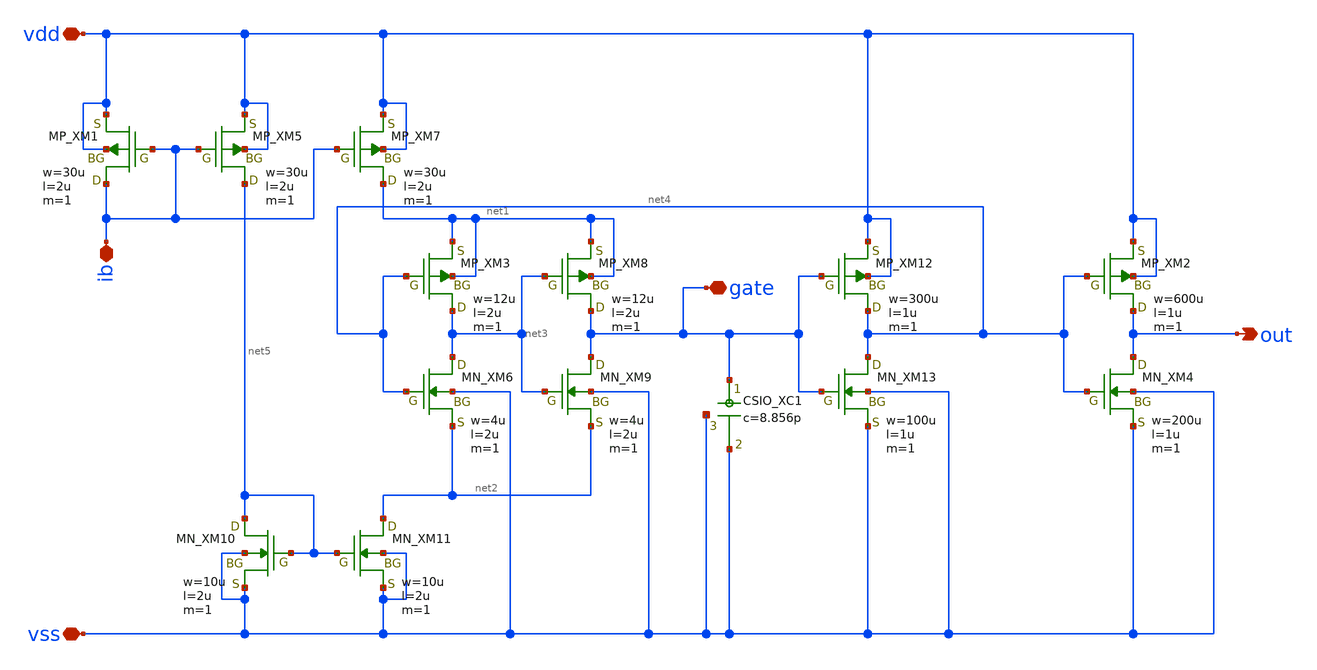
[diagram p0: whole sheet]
** sch_path: Vol.2/files/06/xschem/vco.sch
**.subckt vco out vdd vss ib gate
*.opin out
*.iopin vdd
*.iopin vss
*.iopin ib
*.iopin gate
XM1 ib ib vdd vdd PMOS w=30u l=2u as=0 ad=0 ps=0 pd=0 nrd=0 nrs=0 m=1
XM3 net3 net4 net1 net1 PMOS w=12u l=2u as=0 ad=0 ps=0 pd=0 nrd=0 nrs=0 m=1
XM6 net3 net4 net2 vss NMOS w=4u l=2u as=0 ad=0 ps=0 pd=0 nrd=0 nrs=0 m=1
XM7 net1 ib vdd vdd PMOS w=30u l=2u as=0 ad=0 ps=0 pd=0 nrd=0 nrs=0 m=1
XM8 gate net3 net1 net1 PMOS w=12u l=2u as=0 ad=0 ps=0 pd=0 nrd=0 nrs=0 m=1
XM9 gate net3 net2 vss NMOS w=4u l=2u as=0 ad=0 ps=0 pd=0 nrd=0 nrs=0 m=1
XM12 net4 gate vdd vdd PMOS w=300u l=1u as=0 ad=0 ps=0 pd=0 nrd=0 nrs=0 m=1
XM13 net4 gate vss vss NMOS w=100u l=1u as=0 ad=0 ps=0 pd=0 nrd=0 nrs=0 m=1
XM2 out net4 vdd vdd PMOS w=600u l=1u as=0 ad=0 ps=0 pd=0 nrd=0 nrs=0 m=1
XM4 out net4 vss vss NMOS w=200u l=1u as=0 ad=0 ps=0 pd=0 nrd=0 nrs=0 m=1
XM5 net5 ib vdd vdd PMOS w=30u l=2u as=0 ad=0 ps=0 pd=0 nrd=0 nrs=0 m=1
XM10 net5 net5 vss vss NMOS w=10u l=2u as=0 ad=0 ps=0 pd=0 nrd=0 nrs=0 m=1
XM11 net2 net5 vss vss NMOS w=10u l=2u as=0 ad=0 ps=0 pd=0 nrd=0 nrs=0 m=1
XC1 gate vss vss F_CSIO c=8.856p x=120u y=120u m=1
**.ends
.end
